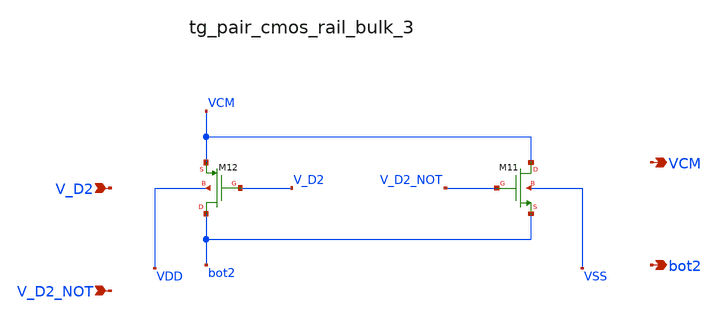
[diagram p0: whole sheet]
** sch_path: analog-db/raw/sw_003_binary_capbank/hier/blocks/tg_pair_cmos_rail_bulk_3.sch
**.subckt tg_pair_cmos_rail_bulk_3 V_D2 V_D2_NOT VCM bot2
*.ipin V_D2
*.ipin V_D2_NOT
*.opin VCM
*.opin bot2
XM11 VCM V_D2_NOT bot2 VSS sg13_lv_nmos w=x_dut_xm11_w l=x_dut_xm11_l ng=1 m=x_dut_xm11_m
XM12 bot2 V_D2 VCM VDD sg13_lv_pmos w=x_dut_xm12_w l=x_dut_xm12_l ng=1 m=x_dut_xm12_m
**.ends
.end
